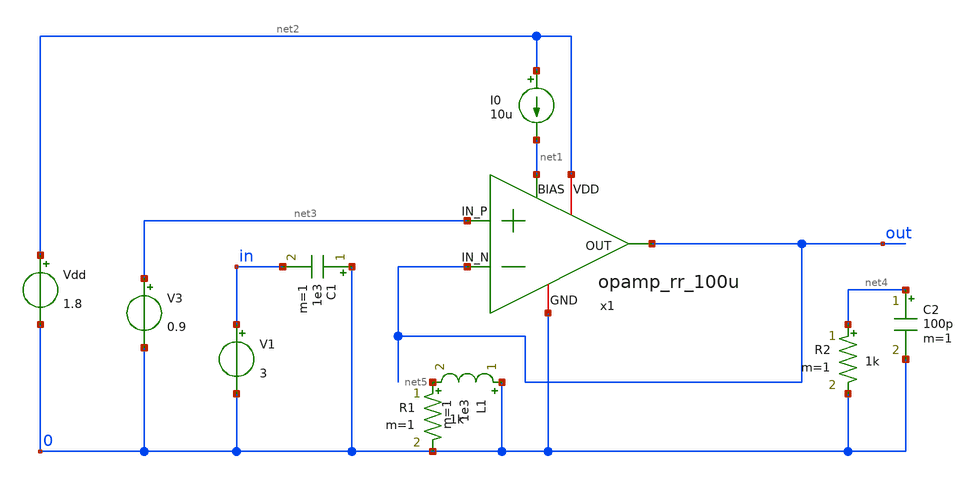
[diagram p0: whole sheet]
** sch_path: design/opamp_rr_100u/tests/opamp_rr_100u_tb.sch
**.subckt opamp_rr_100u_tb
x1 net2 out net1 net3 out 0 opamp_rr_100u w_diffp=30u l_diffp=0.5u m_diffp=2 w_diffn=10u
+ l_diffn=0.5u m_diffn=2 w_casn=1u l_casn=0.5u w_currn=1u l_currn=4u w_curpn=3u l_currp=4u w_casp=3u l_casp=0.5u
+ m_currdiff=4 m_currsec=6 c_compp=0.001p c_compn=0.001p w_outn=10u l_outn=0.5u m_outn=10 w_outp=30u l_outp=0.5u
+ m_outp=10 w_biasp=3u l_biasp=1u m_biasp=1 w_biasn=1u l_biasn=1u m_biasn=1 r_biasn=30k r_biasp=30k
I0 net2 net1 10u
L1 0 net5 1e3 m=1
C1 0 in 1e3 m=1
V1 in 0 3
Vdd net2 0 1.8
C2 net4 0 100p m=1
V3 net3 0 0.9
R1 net5 0 1k m=1
R2 net4 0 1k m=1
**** begin user architecture code


*.option PARHIER=LOCAL RUNLVL=6 post MODMONTE=1 warn maxwarns=400
*.option ITL4=20000 ITL5=0
* .option sampling_method = SRS
* .option method=gear

*.lib xh018/xh018.lib tm
.include 'xh018_ng/xh018.lib'

*.option rshunt = 1.0e3
.option keepopinfo = 1

.temp 30
.tran  6e-7 0.009 uic
.dc Vdd 1.8 1.8 0.25


**** end user architecture code
**.ends

* expanding   symbol:  /home/tom/repositories/amsat_txrx_ic/design/opamp_rr_100u/opamp_rr_100u.sym #
*+ of pins=6
** sym_path: design/opamp_rr_100u/opamp_rr_100u.sym
** sch_path: design/opamp_rr_100u/opamp_rr_100u.sch
.subckt opamp_rr_100u VDD OUT BIAS IN_P IN_N GND  w_diffp=30u l_diffp=0.5u m_diffp=2 w_diffn=10u
+ l_diffn=0.5u m_diffn=2 w_casn=1u l_casn=0.5u w_currn=1u l_currn=4u w_currp=3u l_currp=4u w_casp=3u l_casp=0.5u
+ m_currdiff=4 m_currsec=6 c_compp=0.001p c_compn=0.001p w_outn=10u l_outn=0.5u m_outn=10 w_outp=30u l_outp=0.5u
+ m_outp=10 w_biasp=3u l_biasp=1u m_biasp=1 w_biasn=1u l_biasn=1u m_biasn=1 r_biasn=30k r_biasp=30k
*.ipin BIAS
*.ipin IN_N
*.ipin IN_P
*.opin OUT
*.iopin VDD
*.iopin GND
XMdiffn1 net2 IN_N net6 GND ne w=w_diffn l=l_diffn m=m_diffn
XMdiffp1 net3 IN_N net9 VDD pe w=w_diffp l=l_diffp m=m_diffp
XMcasdiffn1 net6 B_N2 net5 GND ne w=w_casn l=l_casn m=m_currdiff
XMcurrdiffn1 net5 B_N1 GND GND ne w=w_currn l=l_currn m=m_currdiff
XMcasdiffn2 net8 B_N2 net7 GND ne w=w_casn l=l_casn m=m_currdiff
XMcurrdiffn2 net7 B_N1 GND GND ne w=w_currn l=l_currn m=m_currdiff
XMdiffn2 net1 IN_P net8 GND ne w=w_diffn l=l_diffn m=m_diffn
XMcurrdiffp2 net12 B_P1 VDD VDD pe w=w_currp l=l_currp m=m_currdiff
XMcurrdiffp1 net11 B_P1 VDD VDD pe w=w_currp l=l_currp m=m_currdiff
XMcasdiffp2 net10 B_P2 net12 VDD pe w=w_casp l=l_casp m=m_currdiff
XMcasdiffp1 net9 B_P2 net11 VDD pe w=w_casp l=l_casp m=m_currdiff
XMdiffp2 net4 IN_P net10 VDD pe w=w_diffp l=l_diffp m=m_diffp
XMbiasp1 B_N1 B_P3 B_P1 VDD pe w=w_biasp l=l_biasp m=m_biasp
XMcurrsecp2 net1 B_P1 VDD VDD pe w=w_currp l=l_currp m=m_currsec
XMcurrsecp1 net2 B_P1 VDD VDD pe w=w_currp l=l_currp m=m_currsec
XMcassecp2 net14 B_P2 net1 VDD pe w=w_casp l=l_casp m=m_currsec
XMcassecp1 B_P1 B_P2 net2 VDD pe w=w_casp l=l_casp m=m_currsec
XMcassecn1 B_N1 B_N2 net3 GND ne w=w_casn l=l_casn m=m_currsec
XMcurrsecn1 net3 B_N1 GND GND ne w=w_currn l=l_currn m=m_currsec
XMcassecn2 net13 B_N2 net4 GND ne w=w_casn l=l_casn m=m_currsec
XMcurrsecn2 net4 B_N1 GND GND ne w=w_currn l=l_currn m=m_currsec
XMbiasp2 net13 B_P3 net14 VDD pe w=w_biasp l=l_biasp m=m_biasp
XMbiasn1 B_P1 B_N3 B_N1 GND ne w=w_biasn l=l_biasn m=m_biasn
XMbiasn2 net14 B_N3 net13 GND ne w=w_biasn l=l_biasn m=m_biasn
XMbiasoutn net15 net15 GND GND ne w=w_outn l=l_outn m=1
XMbiasn3 B_N3 B_N3 net15 GND ne w=w_biasn l=l_biasn m=1
XMcasp2 B_N3 B_P2 net16 VDD pe w=w_casp l=l_casp m=2
XMcurrp2 net16 B_P1 VDD VDD pe w=w_currp l=l_currp m=2
XMcurrn3 net18 B_N1 GND GND ne w=w_currn l=l_currn m=2
XMcasn3 B_P3 B_N2 net18 GND ne w=w_casn l=l_casn m=2
XMbiasoutp B_P3 B_P3 net17 VDD pe w=w_outp l=l_outp m=1
XMbiasoutp1 net17 net17 VDD VDD pe w=w_outp l=l_outp m=1
XMoutn OUT net13 GND GND ne w=w_outn l=l_outn m=w_outn
XMoutp OUT net14 VDD VDD pe w=w_outp l=l_outp m=w_outp
XMcasn1 B_N1 B_N2 net19 GND ne w=w_casn l=l_casn m=2
XMcurrn1 net19 B_N1 GND GND ne w=w_currn l=l_currn m=2
XMcasn2 B_P2 B_N2 net20 GND ne w=w_casn l=l_casn m=2
XMcurrn2 net20 B_N1 GND GND ne w=w_currn l=l_currn m=2
XMcurrp1 net21 B_P1 VDD VDD pe w=w_currp l=l_currp m=2
XMcasp1 B_P1 B_P2 net21 VDD pe w=w_casp l=l_casp m=2
Rbiasn B_N2 B_N1 {r_biasn} m=1
Rbiasp B_P1 B_P2 {r_biasp} m=1
Ccompn OUT net4 {c_compn} m=1
Ccompp net1 OUT {c_compp} m=1
Rfake B_N2 BIAS 1 m=1
.ends

.end
